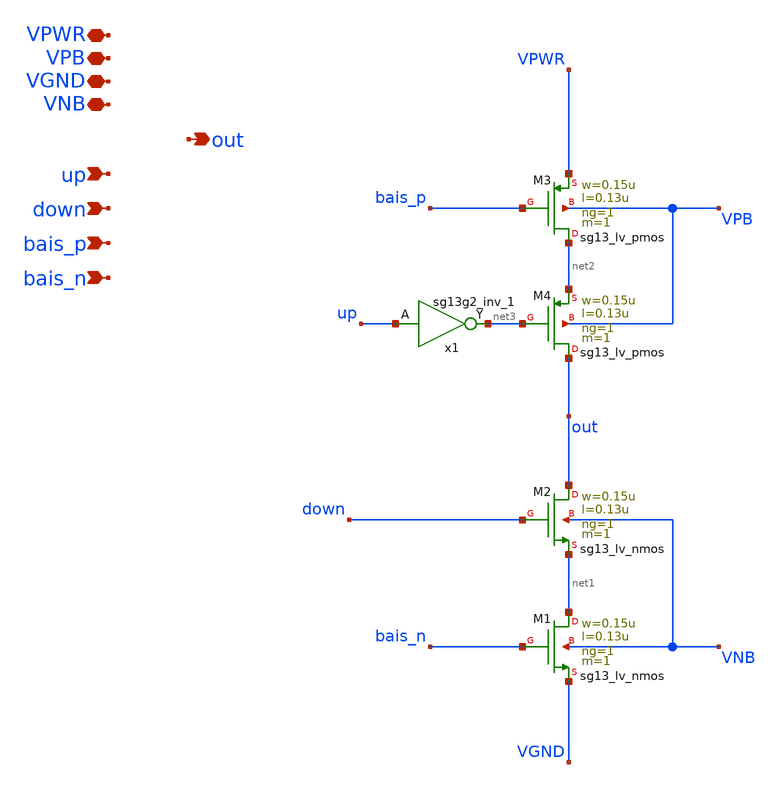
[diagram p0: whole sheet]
** sch_path: Team 2 Design/design_data/xschem/t2_charge_pump.sch
**.subckt t2_charge_pump VPWR up out VPB VGND VNB down bais_p bais_n
*.iopin VPWR
*.ipin up
*.opin out
*.iopin VPB
*.iopin VGND
*.iopin VNB
*.ipin down
*.ipin bais_p
*.ipin bais_n
XM1 net1 bais_n VGND VNB sg13_lv_nmos w=0.15u l=0.13u ng=1 m=1 mm_ok=1
XM2 out down net1 VNB sg13_lv_nmos w=0.15u l=0.13u ng=1 m=1 mm_ok=1
XM3 net2 bais_p VPWR VPB sg13_lv_pmos w=0.15u l=0.13u ng=1 m=1 mm_ok=1
XM4 out net3 net2 VPB sg13_lv_pmos w=0.15u l=0.13u ng=1 m=1 mm_ok=1
x1 net3 up VDD VSS sg13g2_inv_1
**.ends

* expanding   symbol:  sg13g2_stdcells/sg13g2_inv_1.sym # of pins=2
** sym_path: sg13g2_stdcells/sg13g2_inv_1.sym
** sch_path: sg13g2_stdcells/sg13g2_inv_1.sch
.subckt sg13g2_inv_1 Y A VDD VSS
*.opin Y
*.ipin A
*.iopin VDD
*.iopin VSS
XM1 Y A VSS VSS sg13_lv_nmos w=740.00n l=130.00n ng=1 m=1 mm_ok=1
XM2 Y A VDD VDD sg13_lv_pmos w=1.12u l=130.00n ng=1 m=1 mm_ok=1
.ends

.end
